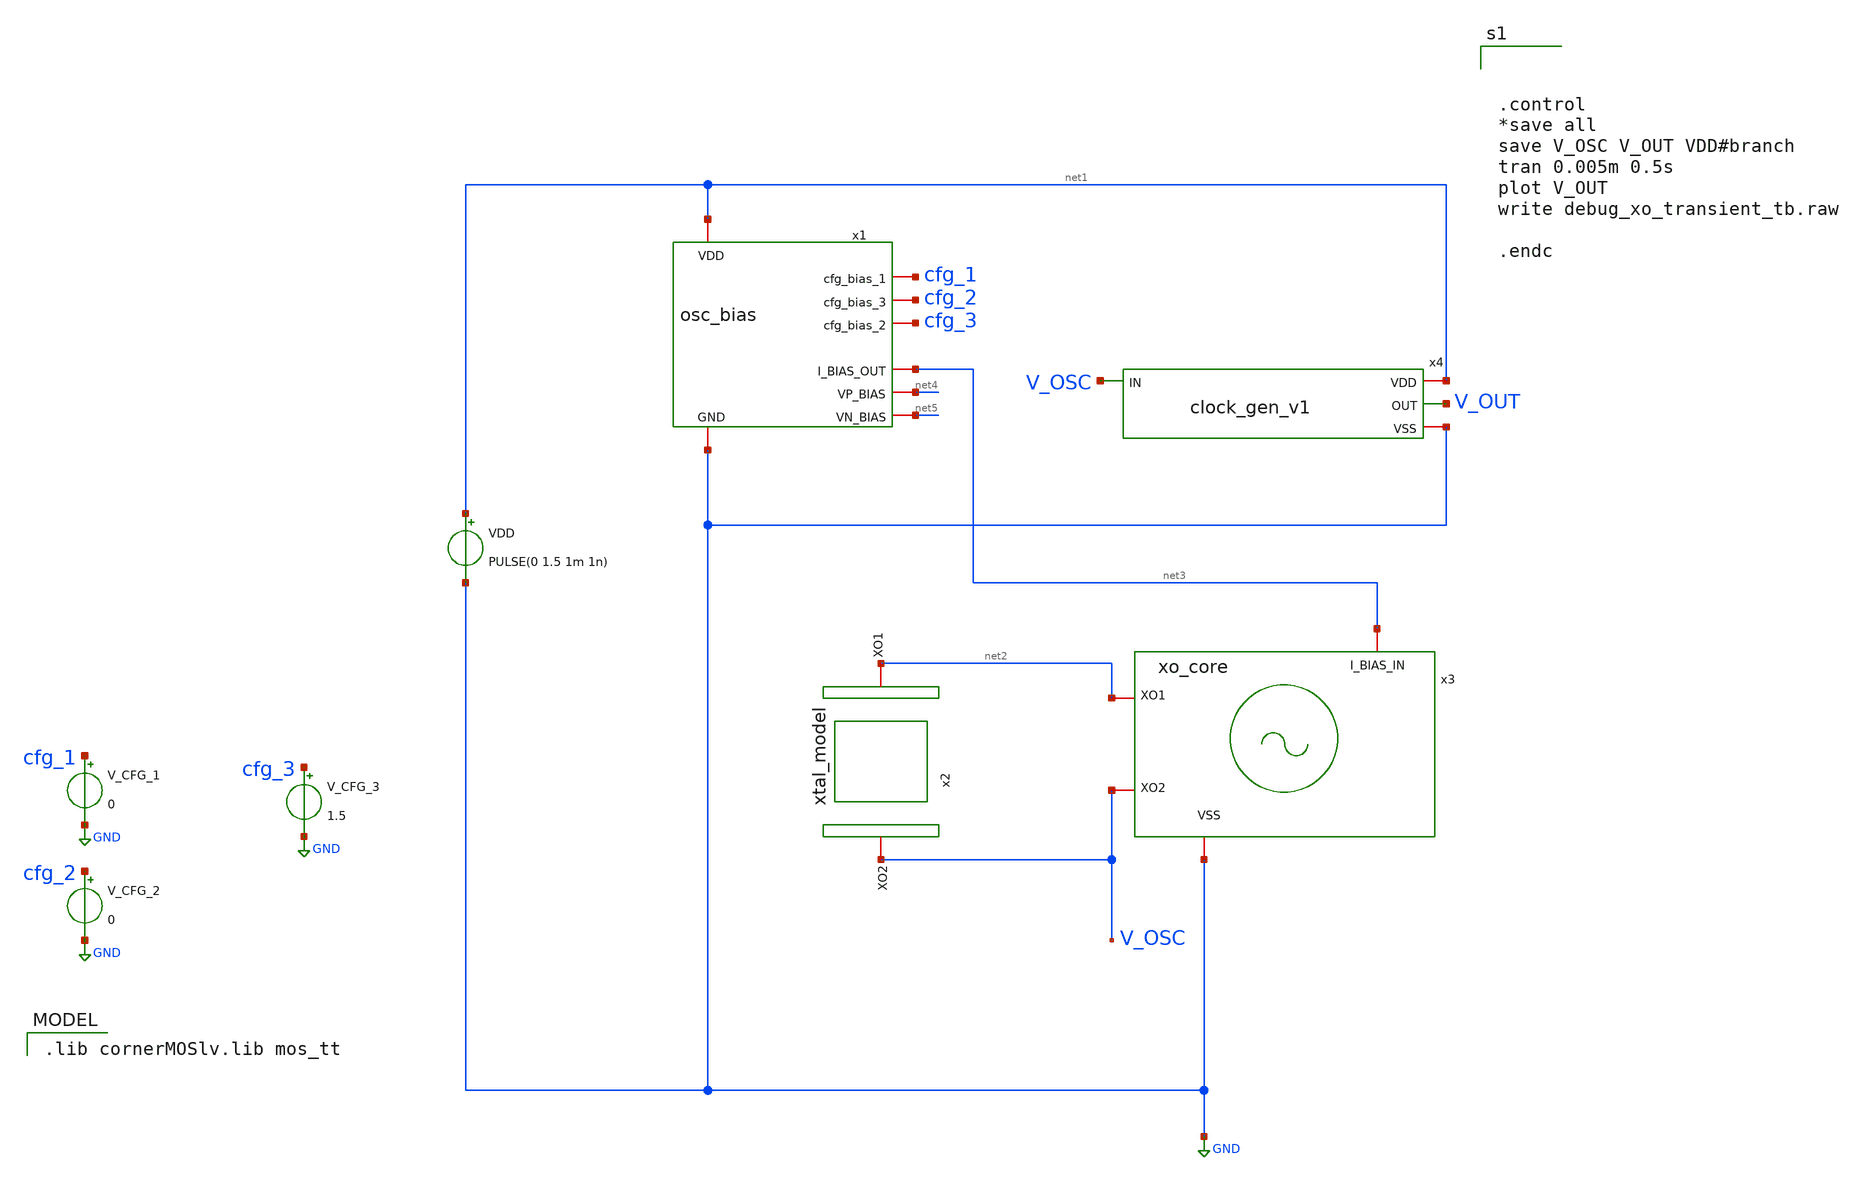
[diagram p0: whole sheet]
** sch_path: debug_xo_transient_tb_v1.sch
**.subckt debug_xo_transient_tb_v1
VDD net1 GND PULSE(0 1.5 1m 1n)
x1 net1 cfg_1 cfg_2 cfg_3 GND net3 net4 net5 osc_bias
x2 net2 V_OSC xtal_model
x3 net3 V_OSC net2 GND xo_core
V_CFG_1 cfg_1 GND 0
V_CFG_2 cfg_2 GND 0
V_CFG_3 cfg_3 GND 1.5
x4 net1 V_OSC V_OUT GND clock_gen_v1
**** begin user architecture code



.control
*save all
save V_OSC V_OUT VDD#branch
tran 0.005m 0.5s
plot V_OUT
write debug_xo_transient_tb.raw

.endc


 .lib cornerMOSlv.lib mos_tt

**** end user architecture code
**.ends

* expanding   symbol:  osc_bias.sym # of pins=8
** sym_path: osc_bias.sym
** sch_path: osc_bias.sch
.subckt osc_bias VDD cfg_bias_1 cfg_bias_3 cfg_bias_2 GND I_BIAS_OUT VP_BIAS VN_BIAS
*.iopin VDD
*.iopin GND
*.iopin I_BIAS_OUT
*.iopin cfg_bias_1
*.iopin cfg_bias_2
*.iopin cfg_bias_3
*.opin VN_BIAS
*.opin VP_BIAS
XM1 VP_BIAS VP_BIAS VDD VDD sg13_lv_pmos w=0.25u l=10u ng=1 m=1 mm_ok=1
XM3 VP_BIAS VP_BIAS net1 GND sg13_lv_nmos w=0.25u l=10u ng=1 m=1 mm_ok=1
XM4 net1 net1 net2 GND sg13_lv_nmos w=0.25u l=10u ng=1 m=1 mm_ok=1
XM5 net2 net2 net7 GND sg13_lv_nmos w=0.25u l=10u ng=1 m=1 mm_ok=1
XM2 net6 VP_BIAS VDD VDD sg13_lv_pmos w=2u l=10u ng=1 m=1 mm_ok=1
XM6 I_BIAS_OUT cfg_bias_1 net6 VDD sg13_lv_pmos w=0.25u l=10u ng=1 m=1 mm_ok=1
XM7 net3 VP_BIAS VDD VDD sg13_lv_pmos w=0.5u l=10u ng=1 m=1 mm_ok=1
XM8 net4 VP_BIAS VDD VDD sg13_lv_pmos w=1u l=10u ng=1 m=1 mm_ok=1
XM9 I_BIAS_OUT cfg_bias_2 net3 VDD sg13_lv_pmos w=0.5u l=10u ng=1 m=1 mm_ok=1
XM10 I_BIAS_OUT cfg_bias_3 net4 VDD sg13_lv_pmos w=1u l=10u ng=1 m=1 mm_ok=1
XM11 VN_BIAS VN_BIAS net5 GND sg13_lv_nmos w=0.25u l=10u ng=1 m=1 mm_ok=1
Vmeas net5 GND 0
.save i(vmeas)
C1 VDD VP_BIAS 1p m=1
R1 VDD VP_BIAS 100Meg m=1
XM12 net7 net7 VN_BIAS GND sg13_lv_nmos w=0.25u l=10u ng=1 m=1 mm_ok=1
.ends


* expanding   symbol:  xtal_model.sym # of pins=2
** sym_path: xtal_model.sym
** sch_path: xtal_model.sch
.subckt xtal_model XO1 XO2
*.iopin XO2
*.iopin XO1
R1 XO1 net1 1k m=1
Cm net1 net2 1p m=1
C0 XO1 XO2 1p m=1
Lm net2 XO2 1n m=1
.ends


* expanding   symbol:  xo_core.sym # of pins=4
** sym_path: xo_core.sym
** sch_path: xo_core.sch
.subckt xo_core I_BIAS_IN XO2 XO1 VSS
*.iopin VSS
*.ipin I_BIAS_IN
*.iopin XO1
*.iopin XO2
XM2 net1 XO1 XO1 XO1 sg13_lv_pmos w=2u l=2u ng=1 m=1 mm_ok=1
XM3 XO2 net1 net1 net1 sg13_lv_pmos w=2u l=2u ng=1 m=1 mm_ok=1
XM1 XO2 XO1 VSS VSS sg13_lv_nmos w=1.0u l=1.0u ng=1 m=1 mm_ok=1
C2 XO2 VSS 8p m=1
C1 XO1 VSS 8p m=1
Vmeas I_BIAS_IN XO2 0
.save i(vmeas)
.ends


* expanding   symbol:  clock_gen_v1.sym # of pins=4
** sym_path: clock_gen_v1.sym
** sch_path: clock_gen_v1.sch
.subckt clock_gen_v1 VDD IN OUT VSS
*.iopin VSS
*.iopin VDD
*.ipin IN
*.opin OUT
XM1 stage_1 net1 net2 VSS sg13_lv_nmos w=1u l=0.13u ng=1 m=1 mm_ok=1
XM2 stage_1 net1 net3 VDD sg13_lv_pmos w=2u l=0.13u ng=1 m=1 mm_ok=1
R1 stage_1 net1 1G m=1
C1 IN net1 10p m=1
XM3 stage_2 stage_1 VSS VSS sg13_lv_nmos w=1u l=0.13u ng=1 m=1 mm_ok=1
XM4 stage_2 stage_1 VDD VDD sg13_lv_pmos w=1u l=0.13u ng=1 m=1 mm_ok=1
XM5 OUT stage_2 VSS VSS sg13_lv_nmos w=1u l=0.13u ng=1 m=1 mm_ok=1
XM6 OUT stage_2 VDD VDD sg13_lv_pmos w=1u l=0.13u ng=1 m=1 mm_ok=1
Vmeas_NMOS net2 VSS 0
.save i(vmeas_nmos)
Vmeas_PMOS net4 net3 0
.save i(vmeas_pmos)
.ends

.GLOBAL GND
.end
